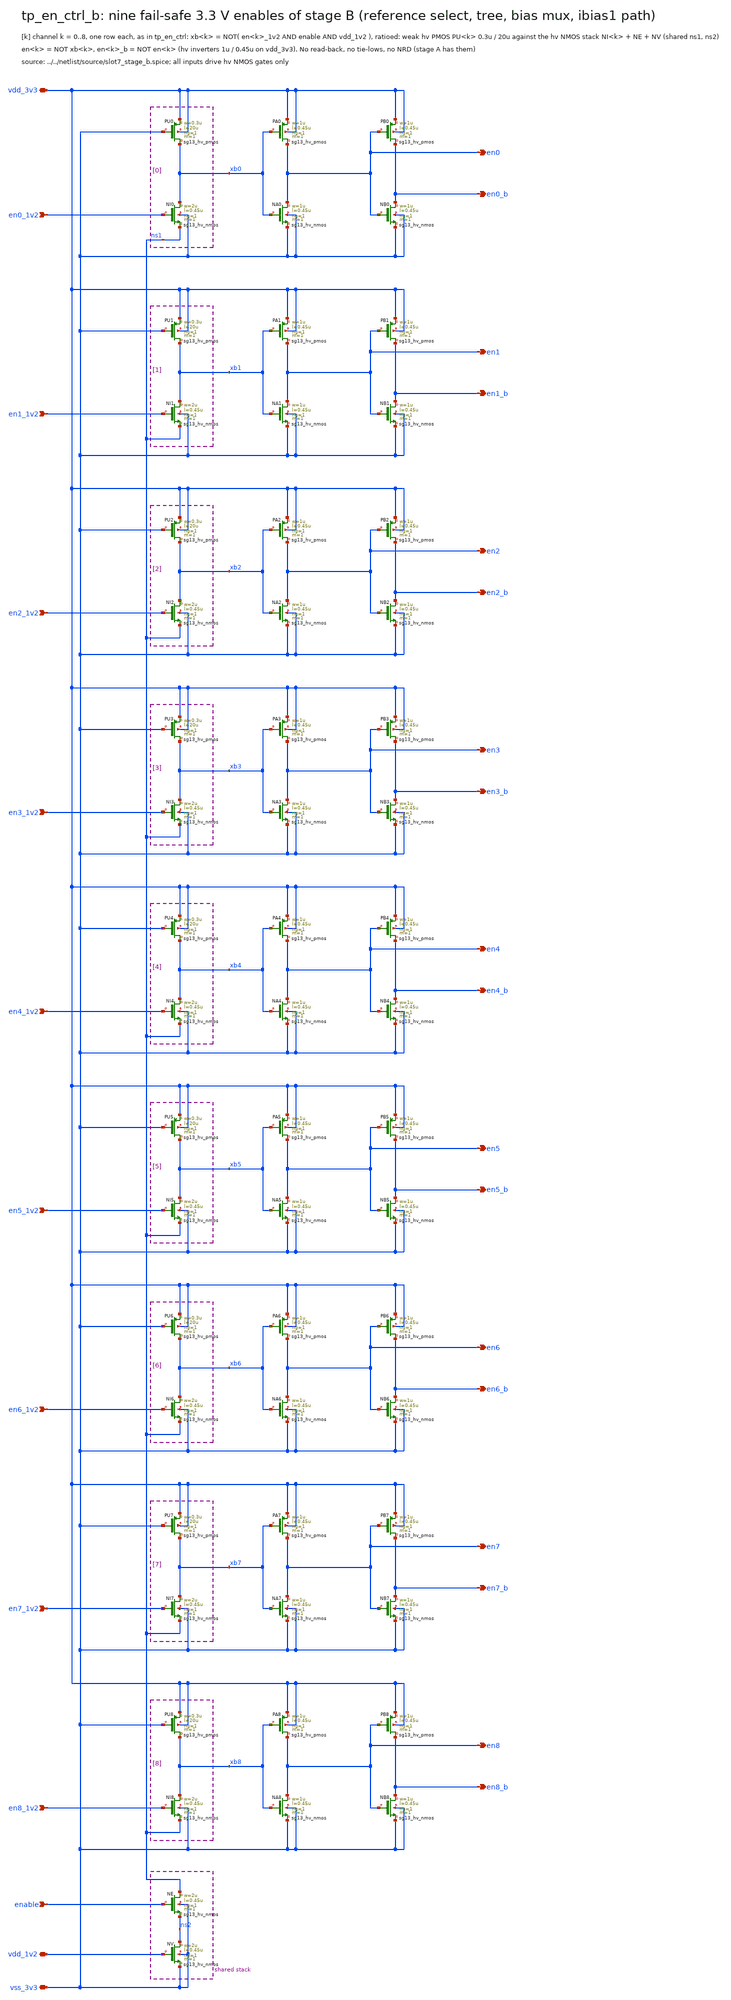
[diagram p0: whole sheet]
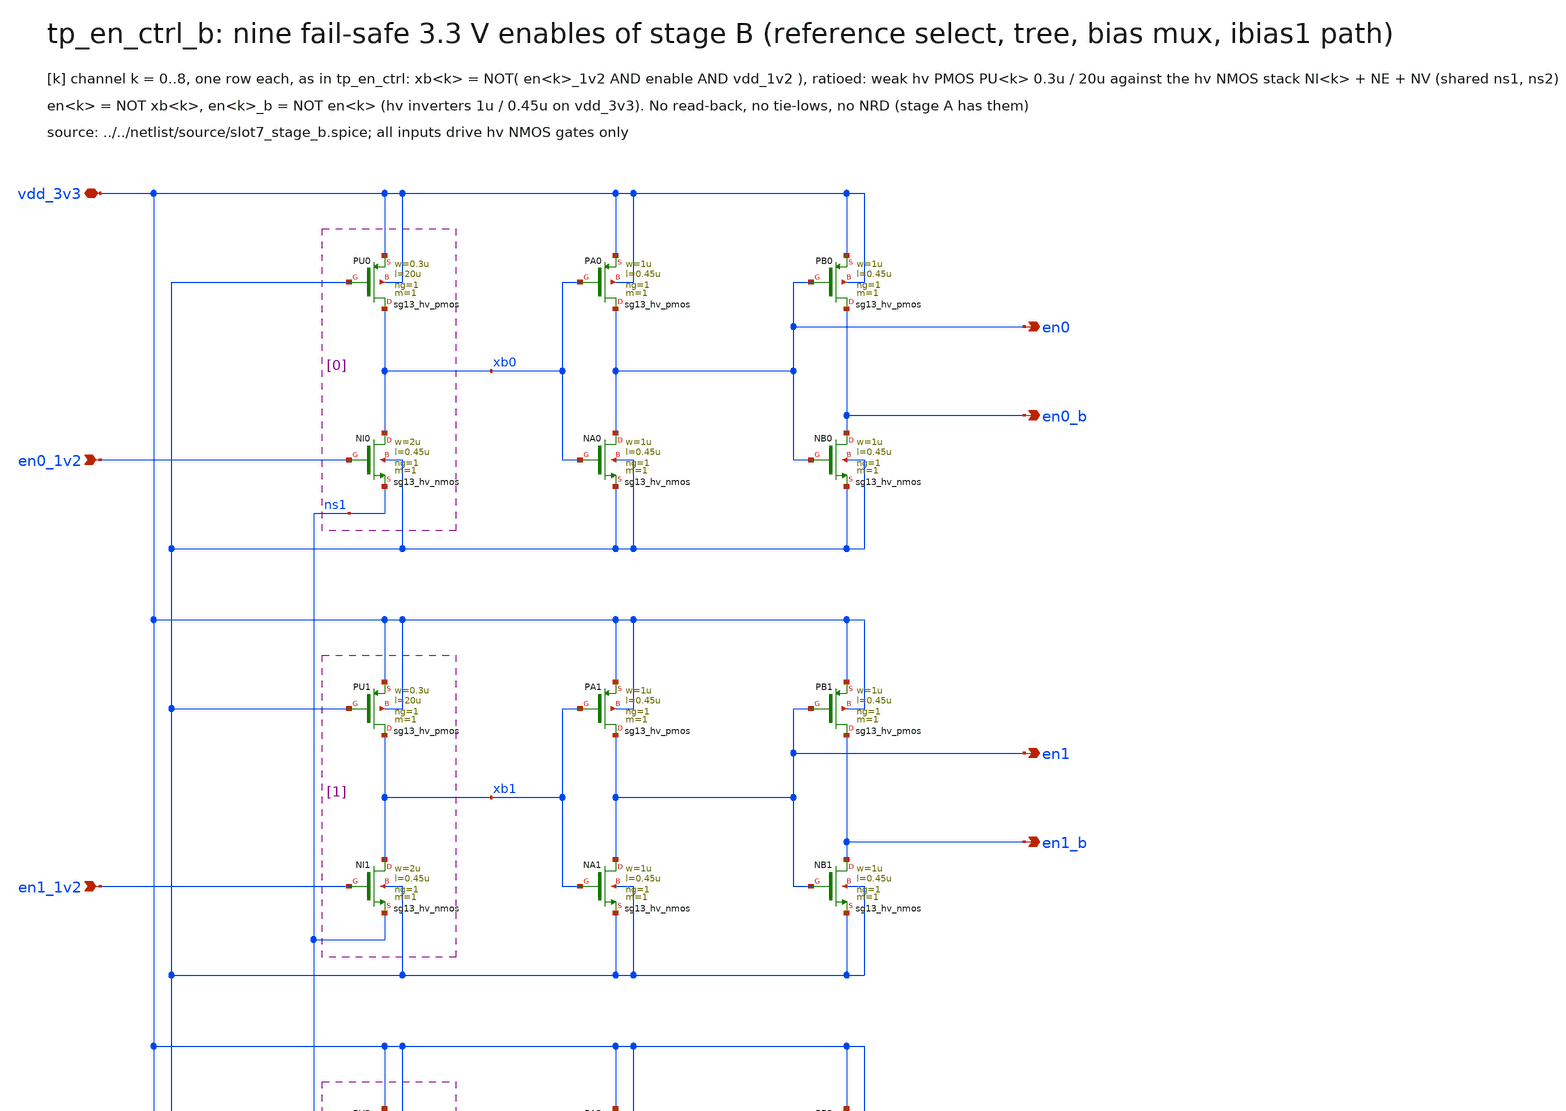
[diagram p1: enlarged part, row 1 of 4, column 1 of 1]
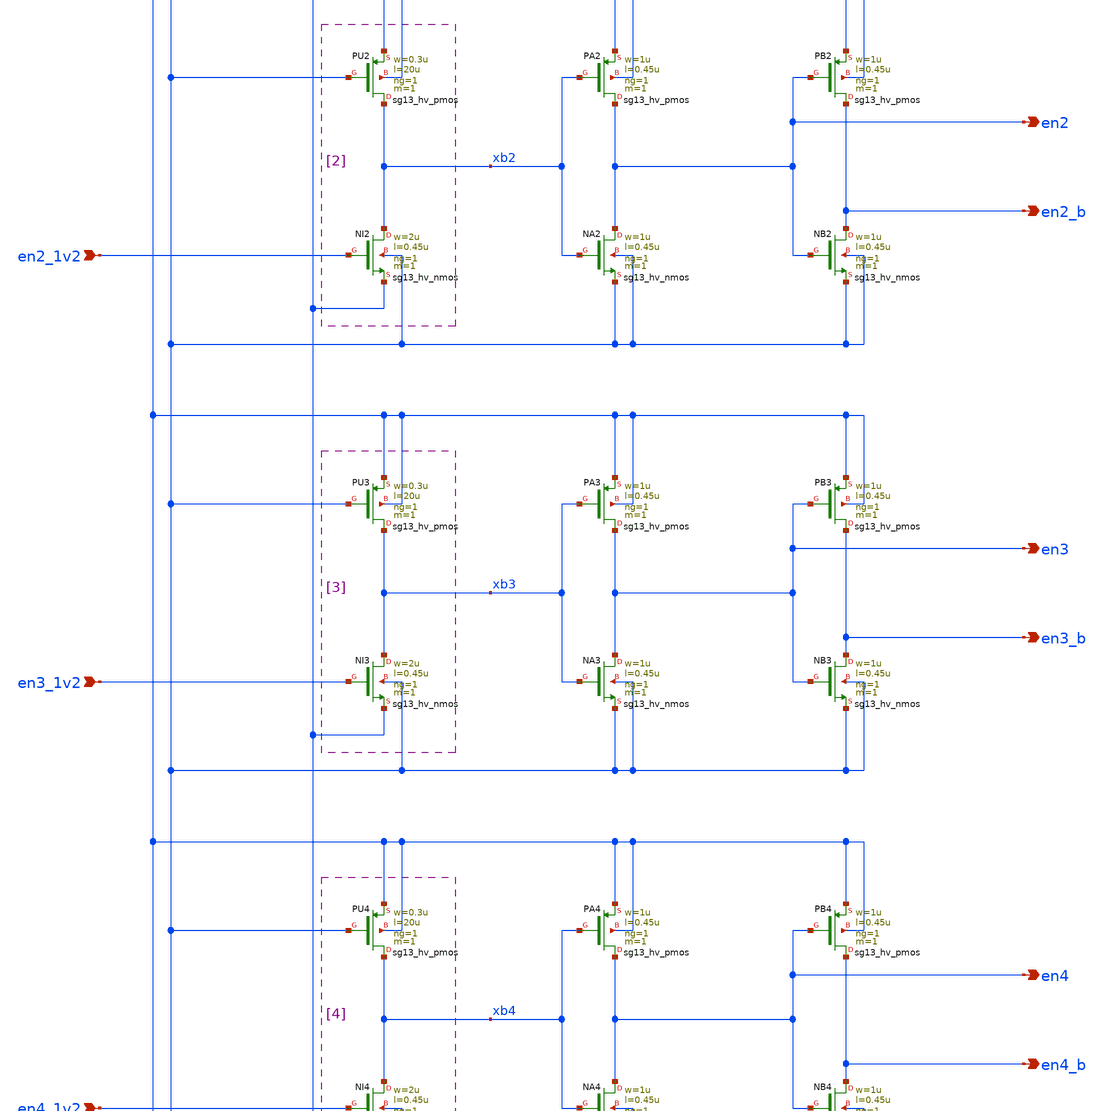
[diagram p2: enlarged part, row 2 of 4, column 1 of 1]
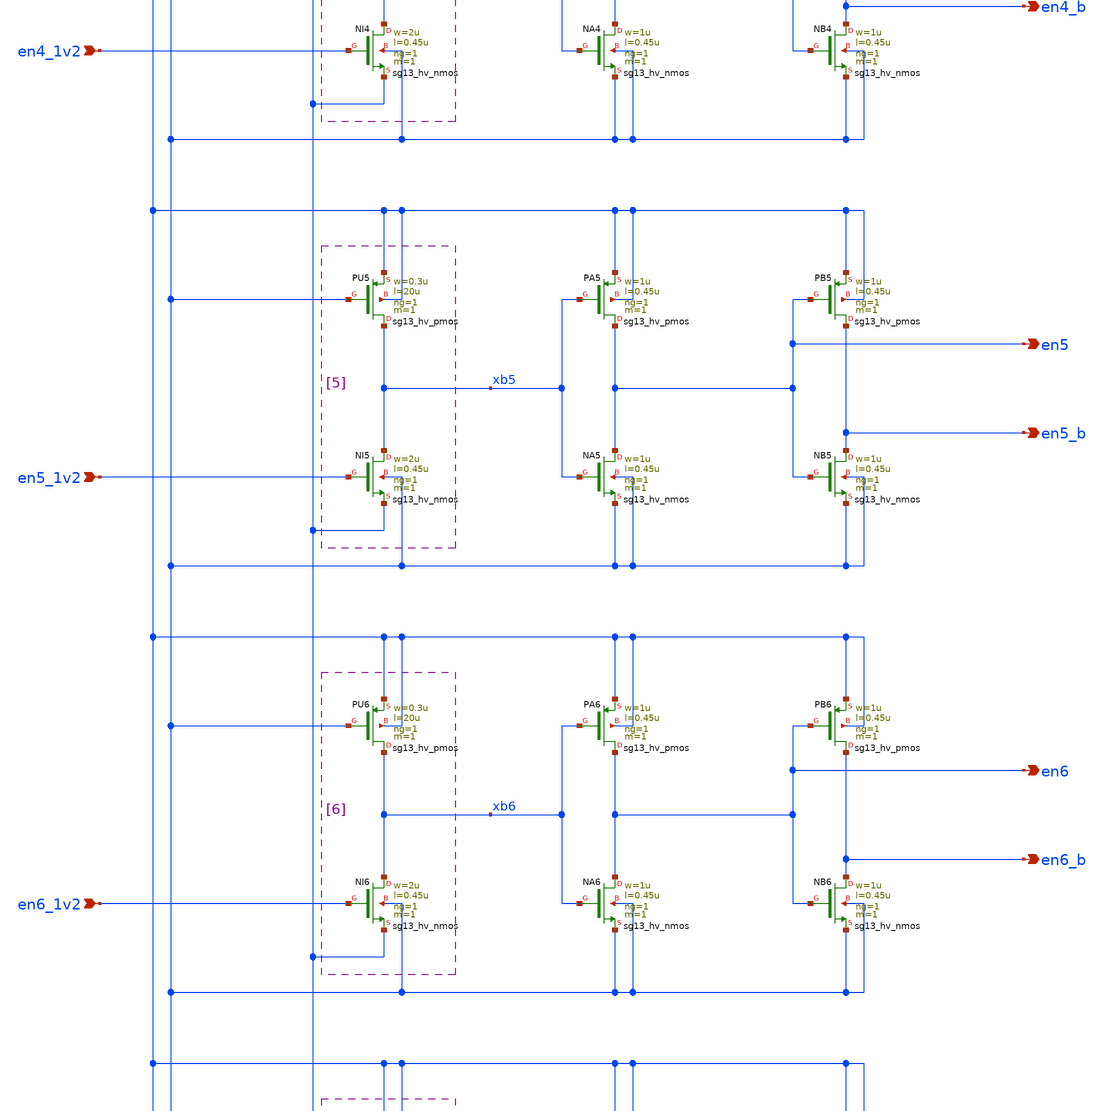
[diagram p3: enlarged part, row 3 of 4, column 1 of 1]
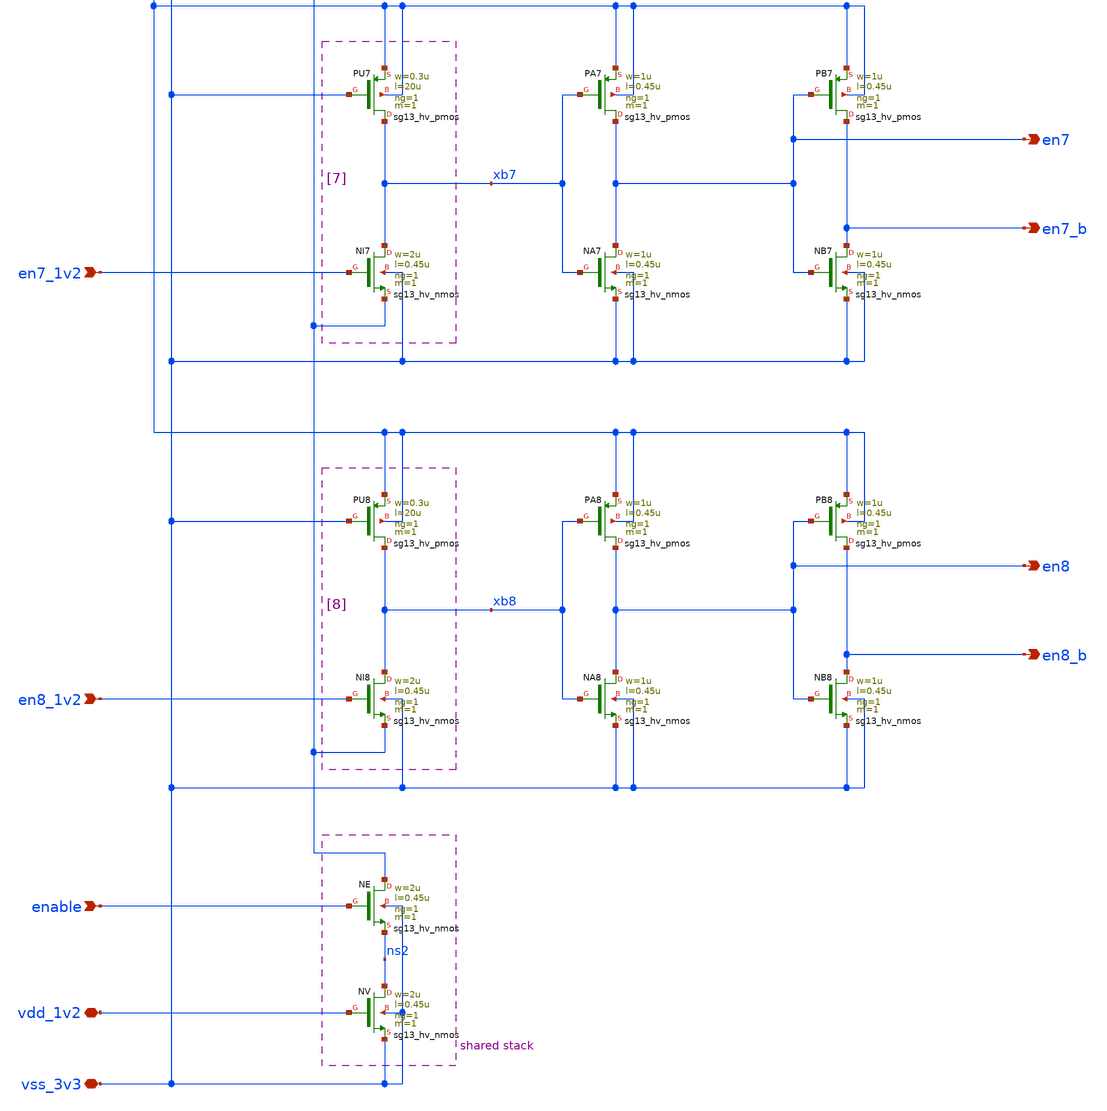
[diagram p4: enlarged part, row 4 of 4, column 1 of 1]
** sch_path: macros/slot7_testplatform/schematic/xschem_drawn/tp_en_ctrl_b.sch
**.subckt tp_en_ctrl_b vdd_3v3 vss_3v3 vdd_1v2 en0_1v2 en1_1v2 en2_1v2 en3_1v2 en4_1v2 en5_1v2
*+ en6_1v2 en7_1v2 en8_1v2 enable en0 en0_b en1 en1_b en2 en2_b en3 en3_b en4 en4_b en5 en5_b en6 en6_b en7
*+ en7_b en8 en8_b
*.iopin vdd_3v3
*.iopin vss_3v3
*.iopin vdd_1v2
*.ipin en0_1v2
*.ipin en1_1v2
*.ipin en2_1v2
*.ipin en3_1v2
*.ipin en4_1v2
*.ipin en5_1v2
*.ipin en6_1v2
*.ipin en7_1v2
*.ipin en8_1v2
*.ipin enable
*.opin en0
*.opin en0_b
*.opin en1
*.opin en1_b
*.opin en2
*.opin en2_b
*.opin en3
*.opin en3_b
*.opin en4
*.opin en4_b
*.opin en5
*.opin en5_b
*.opin en6
*.opin en6_b
*.opin en7
*.opin en7_b
*.opin en8
*.opin en8_b
XPU0 xb0 vss_3v3 vdd_3v3 vdd_3v3 sg13_hv_pmos w=0.3u l=20u ng=1 m=1 mm_ok=1
XNI0 xb0 en0_1v2 ns1 vss_3v3 sg13_hv_nmos w=2u l=0.45u ng=1 m=1 mm_ok=1
XPA0 en0 xb0 vdd_3v3 vdd_3v3 sg13_hv_pmos w=1u l=0.45u ng=1 m=1 mm_ok=1
XNA0 en0 xb0 vss_3v3 vss_3v3 sg13_hv_nmos w=1u l=0.45u ng=1 m=1 mm_ok=1
XPB0 en0_b en0 vdd_3v3 vdd_3v3 sg13_hv_pmos w=1u l=0.45u ng=1 m=1 mm_ok=1
XNB0 en0_b en0 vss_3v3 vss_3v3 sg13_hv_nmos w=1u l=0.45u ng=1 m=1 mm_ok=1
XPU1 xb1 vss_3v3 vdd_3v3 vdd_3v3 sg13_hv_pmos w=0.3u l=20u ng=1 m=1 mm_ok=1
XNI1 xb1 en1_1v2 ns1 vss_3v3 sg13_hv_nmos w=2u l=0.45u ng=1 m=1 mm_ok=1
XPA1 en1 xb1 vdd_3v3 vdd_3v3 sg13_hv_pmos w=1u l=0.45u ng=1 m=1 mm_ok=1
XNA1 en1 xb1 vss_3v3 vss_3v3 sg13_hv_nmos w=1u l=0.45u ng=1 m=1 mm_ok=1
XPB1 en1_b en1 vdd_3v3 vdd_3v3 sg13_hv_pmos w=1u l=0.45u ng=1 m=1 mm_ok=1
XNB1 en1_b en1 vss_3v3 vss_3v3 sg13_hv_nmos w=1u l=0.45u ng=1 m=1 mm_ok=1
XPU2 xb2 vss_3v3 vdd_3v3 vdd_3v3 sg13_hv_pmos w=0.3u l=20u ng=1 m=1 mm_ok=1
XNI2 xb2 en2_1v2 ns1 vss_3v3 sg13_hv_nmos w=2u l=0.45u ng=1 m=1 mm_ok=1
XPA2 en2 xb2 vdd_3v3 vdd_3v3 sg13_hv_pmos w=1u l=0.45u ng=1 m=1 mm_ok=1
XNA2 en2 xb2 vss_3v3 vss_3v3 sg13_hv_nmos w=1u l=0.45u ng=1 m=1 mm_ok=1
XPB2 en2_b en2 vdd_3v3 vdd_3v3 sg13_hv_pmos w=1u l=0.45u ng=1 m=1 mm_ok=1
XNB2 en2_b en2 vss_3v3 vss_3v3 sg13_hv_nmos w=1u l=0.45u ng=1 m=1 mm_ok=1
XPU3 xb3 vss_3v3 vdd_3v3 vdd_3v3 sg13_hv_pmos w=0.3u l=20u ng=1 m=1 mm_ok=1
XNI3 xb3 en3_1v2 ns1 vss_3v3 sg13_hv_nmos w=2u l=0.45u ng=1 m=1 mm_ok=1
XPA3 en3 xb3 vdd_3v3 vdd_3v3 sg13_hv_pmos w=1u l=0.45u ng=1 m=1 mm_ok=1
XNA3 en3 xb3 vss_3v3 vss_3v3 sg13_hv_nmos w=1u l=0.45u ng=1 m=1 mm_ok=1
XPB3 en3_b en3 vdd_3v3 vdd_3v3 sg13_hv_pmos w=1u l=0.45u ng=1 m=1 mm_ok=1
XNB3 en3_b en3 vss_3v3 vss_3v3 sg13_hv_nmos w=1u l=0.45u ng=1 m=1 mm_ok=1
XPU4 xb4 vss_3v3 vdd_3v3 vdd_3v3 sg13_hv_pmos w=0.3u l=20u ng=1 m=1 mm_ok=1
XNI4 xb4 en4_1v2 ns1 vss_3v3 sg13_hv_nmos w=2u l=0.45u ng=1 m=1 mm_ok=1
XPA4 en4 xb4 vdd_3v3 vdd_3v3 sg13_hv_pmos w=1u l=0.45u ng=1 m=1 mm_ok=1
XNA4 en4 xb4 vss_3v3 vss_3v3 sg13_hv_nmos w=1u l=0.45u ng=1 m=1 mm_ok=1
XPB4 en4_b en4 vdd_3v3 vdd_3v3 sg13_hv_pmos w=1u l=0.45u ng=1 m=1 mm_ok=1
XNB4 en4_b en4 vss_3v3 vss_3v3 sg13_hv_nmos w=1u l=0.45u ng=1 m=1 mm_ok=1
XPU5 xb5 vss_3v3 vdd_3v3 vdd_3v3 sg13_hv_pmos w=0.3u l=20u ng=1 m=1 mm_ok=1
XNI5 xb5 en5_1v2 ns1 vss_3v3 sg13_hv_nmos w=2u l=0.45u ng=1 m=1 mm_ok=1
XPA5 en5 xb5 vdd_3v3 vdd_3v3 sg13_hv_pmos w=1u l=0.45u ng=1 m=1 mm_ok=1
XNA5 en5 xb5 vss_3v3 vss_3v3 sg13_hv_nmos w=1u l=0.45u ng=1 m=1 mm_ok=1
XPB5 en5_b en5 vdd_3v3 vdd_3v3 sg13_hv_pmos w=1u l=0.45u ng=1 m=1 mm_ok=1
XNB5 en5_b en5 vss_3v3 vss_3v3 sg13_hv_nmos w=1u l=0.45u ng=1 m=1 mm_ok=1
XPU6 xb6 vss_3v3 vdd_3v3 vdd_3v3 sg13_hv_pmos w=0.3u l=20u ng=1 m=1 mm_ok=1
XNI6 xb6 en6_1v2 ns1 vss_3v3 sg13_hv_nmos w=2u l=0.45u ng=1 m=1 mm_ok=1
XPA6 en6 xb6 vdd_3v3 vdd_3v3 sg13_hv_pmos w=1u l=0.45u ng=1 m=1 mm_ok=1
XNA6 en6 xb6 vss_3v3 vss_3v3 sg13_hv_nmos w=1u l=0.45u ng=1 m=1 mm_ok=1
XPB6 en6_b en6 vdd_3v3 vdd_3v3 sg13_hv_pmos w=1u l=0.45u ng=1 m=1 mm_ok=1
XNB6 en6_b en6 vss_3v3 vss_3v3 sg13_hv_nmos w=1u l=0.45u ng=1 m=1 mm_ok=1
XPU7 xb7 vss_3v3 vdd_3v3 vdd_3v3 sg13_hv_pmos w=0.3u l=20u ng=1 m=1 mm_ok=1
XNI7 xb7 en7_1v2 ns1 vss_3v3 sg13_hv_nmos w=2u l=0.45u ng=1 m=1 mm_ok=1
XPA7 en7 xb7 vdd_3v3 vdd_3v3 sg13_hv_pmos w=1u l=0.45u ng=1 m=1 mm_ok=1
XNA7 en7 xb7 vss_3v3 vss_3v3 sg13_hv_nmos w=1u l=0.45u ng=1 m=1 mm_ok=1
XPB7 en7_b en7 vdd_3v3 vdd_3v3 sg13_hv_pmos w=1u l=0.45u ng=1 m=1 mm_ok=1
XNB7 en7_b en7 vss_3v3 vss_3v3 sg13_hv_nmos w=1u l=0.45u ng=1 m=1 mm_ok=1
XPU8 xb8 vss_3v3 vdd_3v3 vdd_3v3 sg13_hv_pmos w=0.3u l=20u ng=1 m=1 mm_ok=1
XNI8 xb8 en8_1v2 ns1 vss_3v3 sg13_hv_nmos w=2u l=0.45u ng=1 m=1 mm_ok=1
XPA8 en8 xb8 vdd_3v3 vdd_3v3 sg13_hv_pmos w=1u l=0.45u ng=1 m=1 mm_ok=1
XNA8 en8 xb8 vss_3v3 vss_3v3 sg13_hv_nmos w=1u l=0.45u ng=1 m=1 mm_ok=1
XPB8 en8_b en8 vdd_3v3 vdd_3v3 sg13_hv_pmos w=1u l=0.45u ng=1 m=1 mm_ok=1
XNB8 en8_b en8 vss_3v3 vss_3v3 sg13_hv_nmos w=1u l=0.45u ng=1 m=1 mm_ok=1
XNE ns1 enable ns2 vss_3v3 sg13_hv_nmos w=2u l=0.45u ng=1 m=1 mm_ok=1
XNV ns2 vdd_1v2 vss_3v3 vss_3v3 sg13_hv_nmos w=2u l=0.45u ng=1 m=1 mm_ok=1
**.ends
.end
